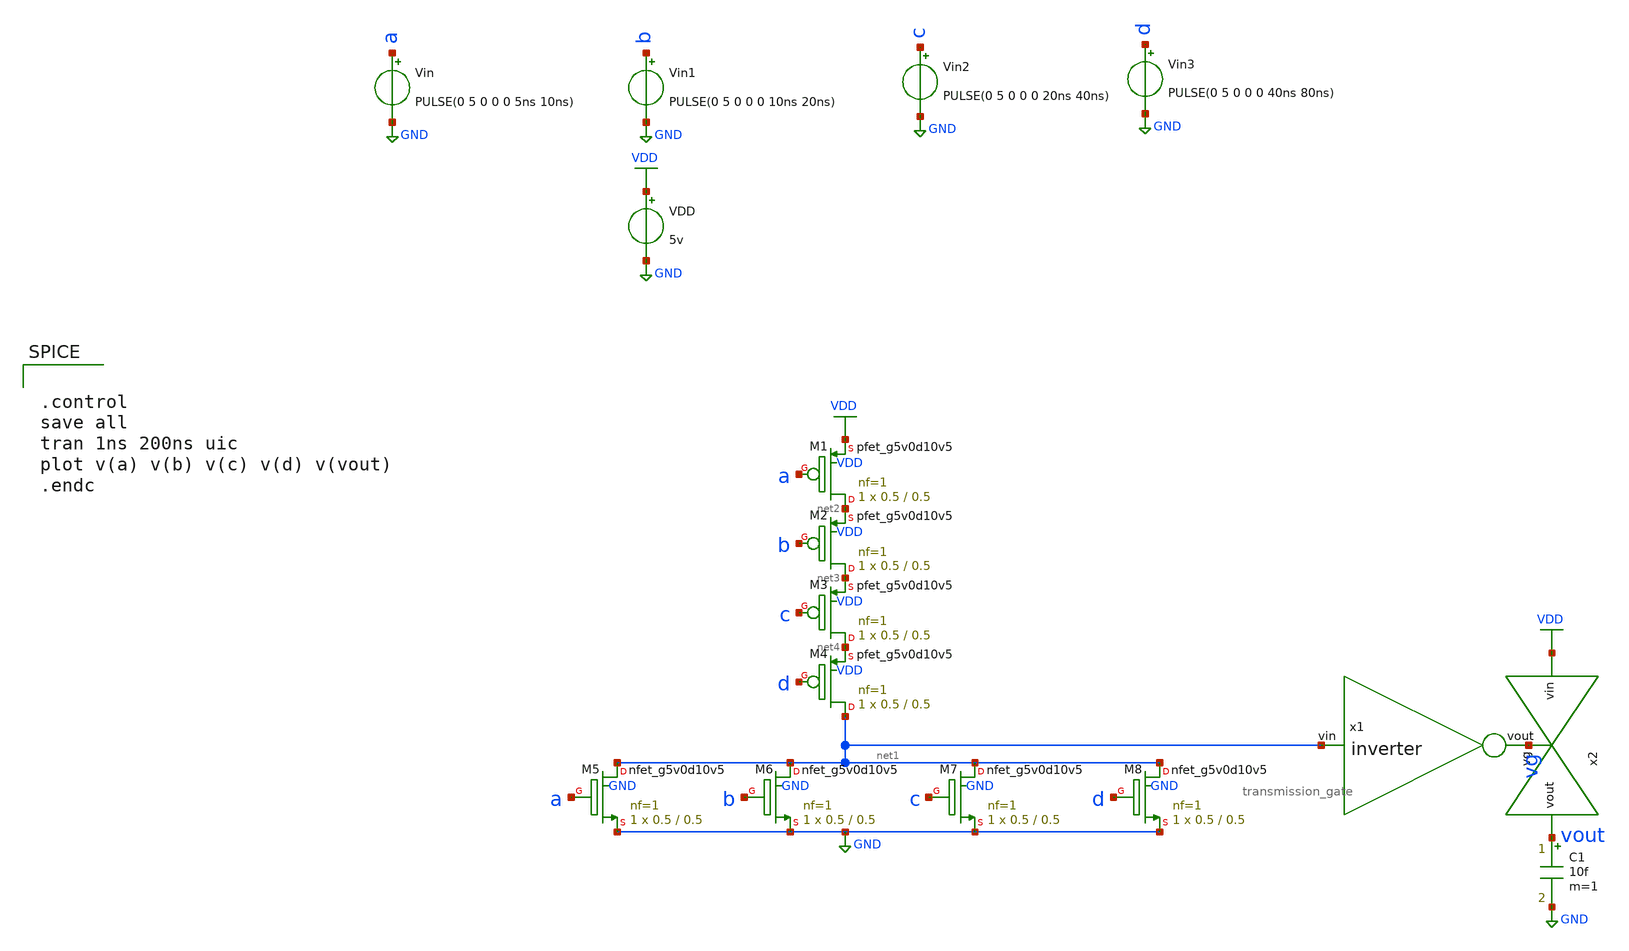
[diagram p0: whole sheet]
** sch_path: schematics/or4_tb.sch
**.subckt or4_tb
Vin a GND PULSE(0 5 0 0 0 5ns 10ns)
VDD VDD GND 5v
Vin1 b GND PULSE(0 5 0 0 0 10ns 20ns)
Vin2 c GND PULSE(0 5 0 0 0 20ns 40ns)
Vin3 d GND PULSE(0 5 0 0 0 40ns 80ns)
x1 vg net1 inverter
XM1 net2 a VDD VDD sky130_fd_pr__pfet_g5v0d10v5 L=0.5 W=0.5 nf=1 ad='int((nf+1)/2) * W/nf * 0.29' as='int((nf+2)/2) * W/nf * 0.29'
+ pd='2*int((nf+1)/2) * (W/nf + 0.29)' ps='2*int((nf+2)/2) * (W/nf + 0.29)' nrd='0.29 / W' nrs='0.29 / W'
+ sa=0 sb=0 sd=0 mult=1 m=1
XM5 net1 a GND GND sky130_fd_pr__nfet_g5v0d10v5 L=0.5 W=0.5 nf=1 ad='int((nf+1)/2) * W/nf * 0.29' as='int((nf+2)/2) * W/nf * 0.29'
+ pd='2*int((nf+1)/2) * (W/nf + 0.29)' ps='2*int((nf+2)/2) * (W/nf + 0.29)' nrd='0.29 / W' nrs='0.29 / W'
+ sa=0 sb=0 sd=0 mult=1 m=1
XM2 net3 b net2 VDD sky130_fd_pr__pfet_g5v0d10v5 L=0.5 W=0.5 nf=1 ad='int((nf+1)/2) * W/nf * 0.29' as='int((nf+2)/2) * W/nf * 0.29'
+ pd='2*int((nf+1)/2) * (W/nf + 0.29)' ps='2*int((nf+2)/2) * (W/nf + 0.29)' nrd='0.29 / W' nrs='0.29 / W'
+ sa=0 sb=0 sd=0 mult=1 m=1
XM3 net4 c net3 VDD sky130_fd_pr__pfet_g5v0d10v5 L=0.5 W=0.5 nf=1 ad='int((nf+1)/2) * W/nf * 0.29' as='int((nf+2)/2) * W/nf * 0.29'
+ pd='2*int((nf+1)/2) * (W/nf + 0.29)' ps='2*int((nf+2)/2) * (W/nf + 0.29)' nrd='0.29 / W' nrs='0.29 / W'
+ sa=0 sb=0 sd=0 mult=1 m=1
XM4 net1 d net4 VDD sky130_fd_pr__pfet_g5v0d10v5 L=0.5 W=0.5 nf=1 ad='int((nf+1)/2) * W/nf * 0.29' as='int((nf+2)/2) * W/nf * 0.29'
+ pd='2*int((nf+1)/2) * (W/nf + 0.29)' ps='2*int((nf+2)/2) * (W/nf + 0.29)' nrd='0.29 / W' nrs='0.29 / W'
+ sa=0 sb=0 sd=0 mult=1 m=1
XM6 net1 b GND GND sky130_fd_pr__nfet_g5v0d10v5 L=0.5 W=0.5 nf=1 ad='int((nf+1)/2) * W/nf * 0.29' as='int((nf+2)/2) * W/nf * 0.29'
+ pd='2*int((nf+1)/2) * (W/nf + 0.29)' ps='2*int((nf+2)/2) * (W/nf + 0.29)' nrd='0.29 / W' nrs='0.29 / W'
+ sa=0 sb=0 sd=0 mult=1 m=1
XM7 net1 c GND GND sky130_fd_pr__nfet_g5v0d10v5 L=0.5 W=0.5 nf=1 ad='int((nf+1)/2) * W/nf * 0.29' as='int((nf+2)/2) * W/nf * 0.29'
+ pd='2*int((nf+1)/2) * (W/nf + 0.29)' ps='2*int((nf+2)/2) * (W/nf + 0.29)' nrd='0.29 / W' nrs='0.29 / W'
+ sa=0 sb=0 sd=0 mult=1 m=1
XM8 net1 d GND GND sky130_fd_pr__nfet_g5v0d10v5 L=0.5 W=0.5 nf=1 ad='int((nf+1)/2) * W/nf * 0.29' as='int((nf+2)/2) * W/nf * 0.29'
+ pd='2*int((nf+1)/2) * (W/nf + 0.29)' ps='2*int((nf+2)/2) * (W/nf + 0.29)' nrd='0.29 / W' nrs='0.29 / W'
+ sa=0 sb=0 sd=0 mult=1 m=1
x2 VDD vout vg transmission_gate
C1 vout GND 10f m=1
**** begin user architecture code


.control
save all
tran 1ns 200ns uic
plot v(a) v(b) v(c) v(d) v(vout)
.endc


 .lib $::SKYWATER_MODELS/models/sky130.lib.spice tt

.param mc_mm_switch=0
.param mc_pr_switch=1

**** end user architecture code
**.ends

* expanding   symbol:  /media/sf_share/final_project/inverter.sym # of pins=2
** sym_path: schematics/inverter.sym
** sch_path: schematics/inverter.sch
.subckt inverter vout vin
*.ipin vin
*.opin vout
XM3 vout vin VDD VDD sky130_fd_pr__pfet_g5v0d10v5 L=0.5 W=0.5 nf=1 ad='int((nf+1)/2) * W/nf * 0.29' as='int((nf+2)/2) * W/nf * 0.29'
+ pd='2*int((nf+1)/2) * (W/nf + 0.29)' ps='2*int((nf+2)/2) * (W/nf + 0.29)' nrd='0.29 / W' nrs='0.29 / W'
+ sa=0 sb=0 sd=0 mult=1 m=1
XM5 vout vin GND GND sky130_fd_pr__nfet_g5v0d10v5 L=0.5 W=0.5 nf=1 ad='int((nf+1)/2) * W/nf * 0.29' as='int((nf+2)/2) * W/nf * 0.29'
+ pd='2*int((nf+1)/2) * (W/nf + 0.29)' ps='2*int((nf+2)/2) * (W/nf + 0.29)' nrd='0.29 / W' nrs='0.29 / W'
+ sa=0 sb=0 sd=0 mult=1 m=1
.ends


* expanding   symbol:  /media/sf_share/final_project/transmission_gate.sym # of pins=3
** sym_path: schematics/transmission_gate.sym
** sch_path: schematics/transmission_gate.sch
.subckt transmission_gate vin vout vg
*.ipin vin
*.ipin vg
*.opin vout
x1 vg_bar vg inverter
XM5 vin vg vout GND sky130_fd_pr__nfet_g5v0d10v5 L=0.5 W=0.5 nf=1 ad='int((nf+1)/2) * W/nf * 0.29' as='int((nf+2)/2) * W/nf * 0.29'
+ pd='2*int((nf+1)/2) * (W/nf + 0.29)' ps='2*int((nf+2)/2) * (W/nf + 0.29)' nrd='0.29 / W' nrs='0.29 / W'
+ sa=0 sb=0 sd=0 mult=1 m=1
XM7 vout vg_bar vin VDD sky130_fd_pr__pfet_g5v0d10v5 L=0.5 W=0.5 nf=1 ad='int((nf+1)/2) * W/nf * 0.29'
+ as='int((nf+2)/2) * W/nf * 0.29' pd='2*int((nf+1)/2) * (W/nf + 0.29)' ps='2*int((nf+2)/2) * (W/nf + 0.29)'
+ nrd='0.29 / W' nrs='0.29 / W' sa=0 sb=0 sd=0 mult=1 m=1
XM6 vout vg_bar GND GND sky130_fd_pr__nfet_g5v0d10v5 L=0.5 W=0.5 nf=1 ad='int((nf+1)/2) * W/nf * 0.29'
+ as='int((nf+2)/2) * W/nf * 0.29' pd='2*int((nf+1)/2) * (W/nf + 0.29)' ps='2*int((nf+2)/2) * (W/nf + 0.29)'
+ nrd='0.29 / W' nrs='0.29 / W' sa=0 sb=0 sd=0 mult=1 m=1
.ends

.GLOBAL VDD
.GLOBAL GND
.end
